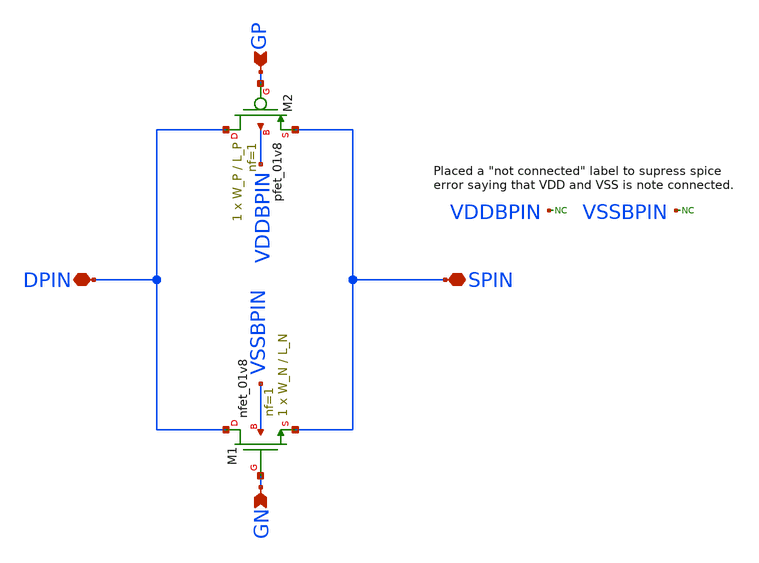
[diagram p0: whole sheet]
** sch_path: transmissiongate.sch
**.subckt transmissiongate DPIN SPIN GP GN
*.iopin DPIN
*.iopin SPIN
*.ipin GP
*.ipin GN
XM1 DPIN GN SPIN VSSBPIN sky130_fd_pr__nfet_01v8 L=L_N W=W_N nf=1 ad='int((nf+1)/2) * W/nf * 0.29' as='int((nf+2)/2) * W/nf * 0.29'
+ pd='2*int((nf+1)/2) * (W/nf + 0.29)' ps='2*int((nf+2)/2) * (W/nf + 0.29)' nrd='0.29 / W' nrs='0.29 / W'
+ sa=0 sb=0 sd=0 mult=1 m=1
XM2 DPIN GP SPIN VDDBPIN sky130_fd_pr__pfet_01v8 L=L_P W=W_P nf=1 ad='int((nf+1)/2) * W/nf * 0.29' as='int((nf+2)/2) * W/nf * 0.29'
+ pd='2*int((nf+1)/2) * (W/nf + 0.29)' ps='2*int((nf+2)/2) * (W/nf + 0.29)' nrd='0.29 / W' nrs='0.29 / W'
+ sa=0 sb=0 sd=0 mult=1 m=1
* noconn VDDBPIN
* noconn VSSBPIN
**.ends
.end
